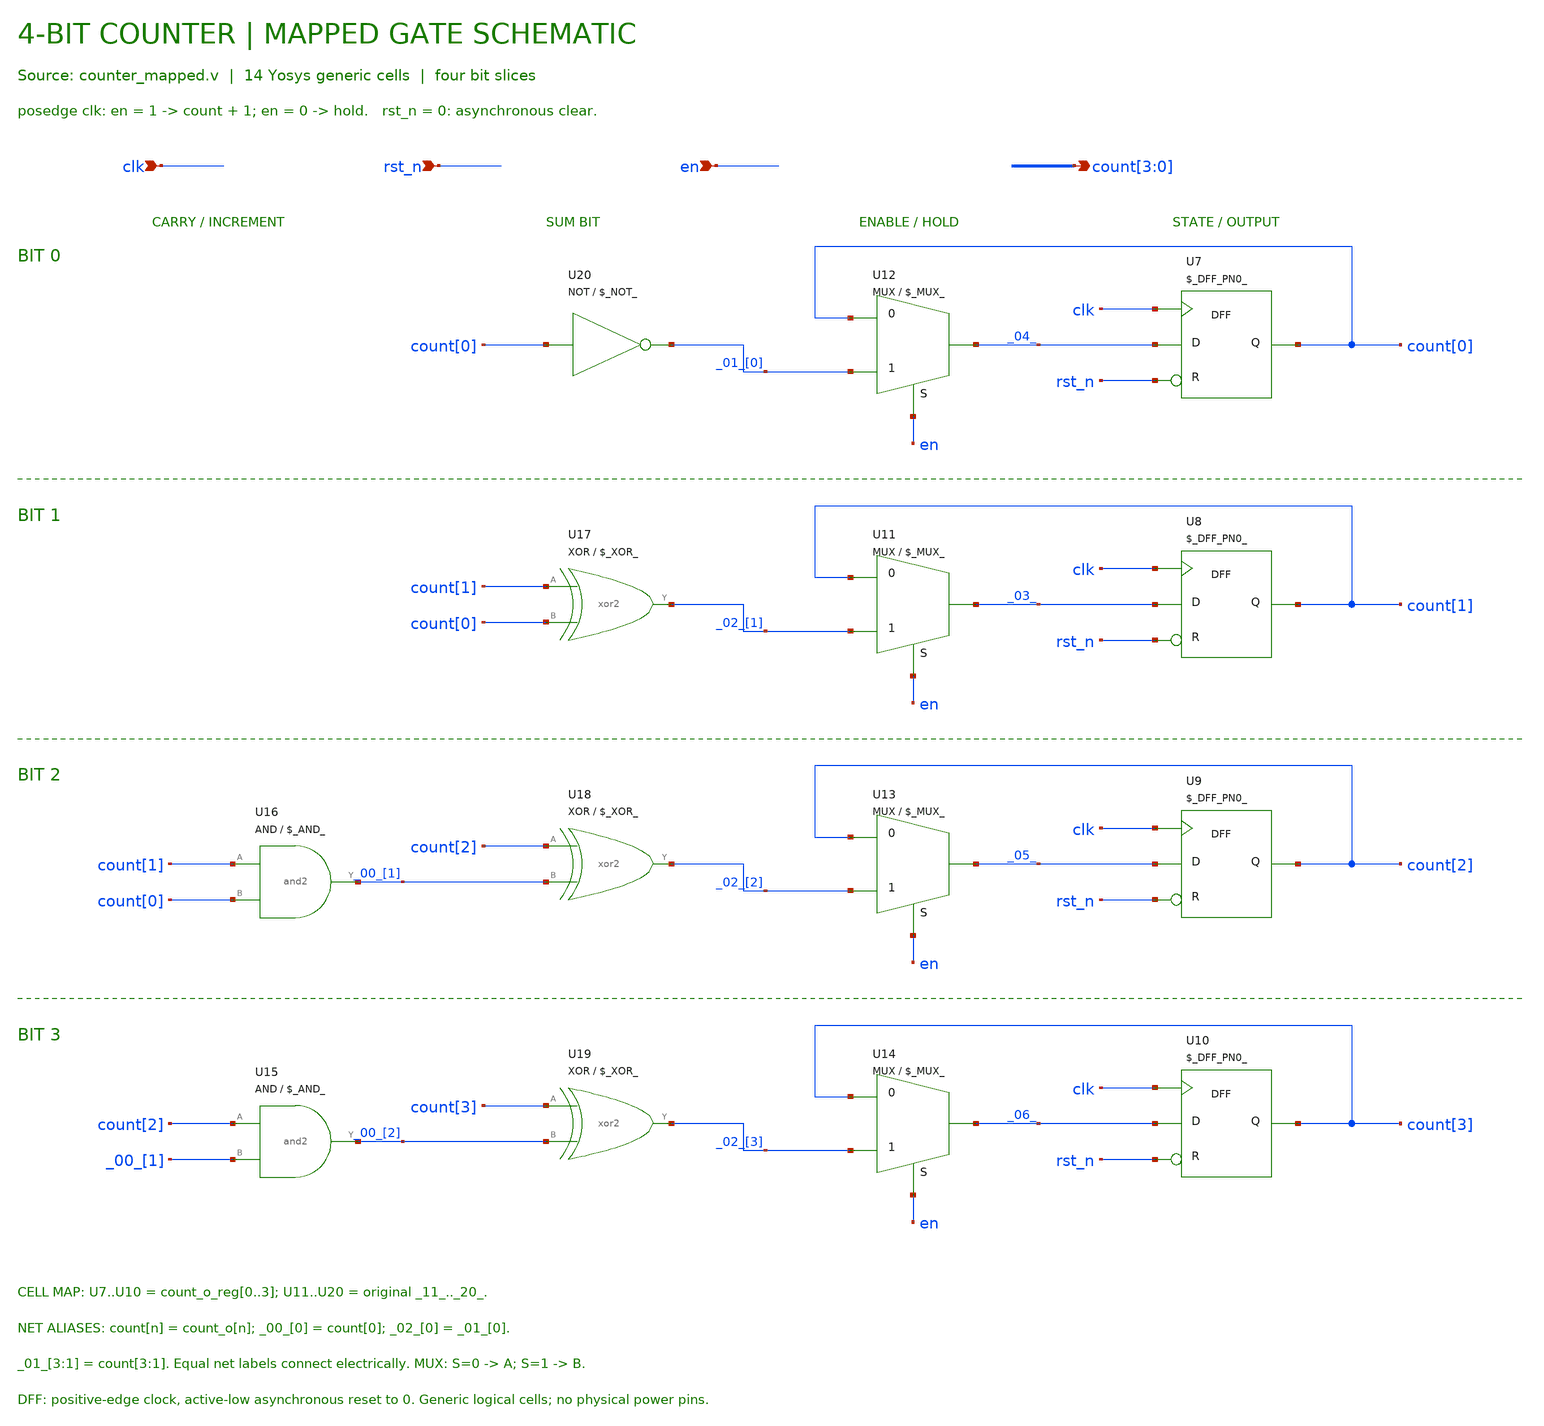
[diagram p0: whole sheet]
** sch_path: examples/counter/counter_dff/counter.sch
**.subckt counter clk rst_n en count[3],count[2],count[1],count[0]
*.ipin clk
*.ipin rst_n
*.ipin en
*.opin count[3],count[2],count[1],count[0]
**.ends
.end
